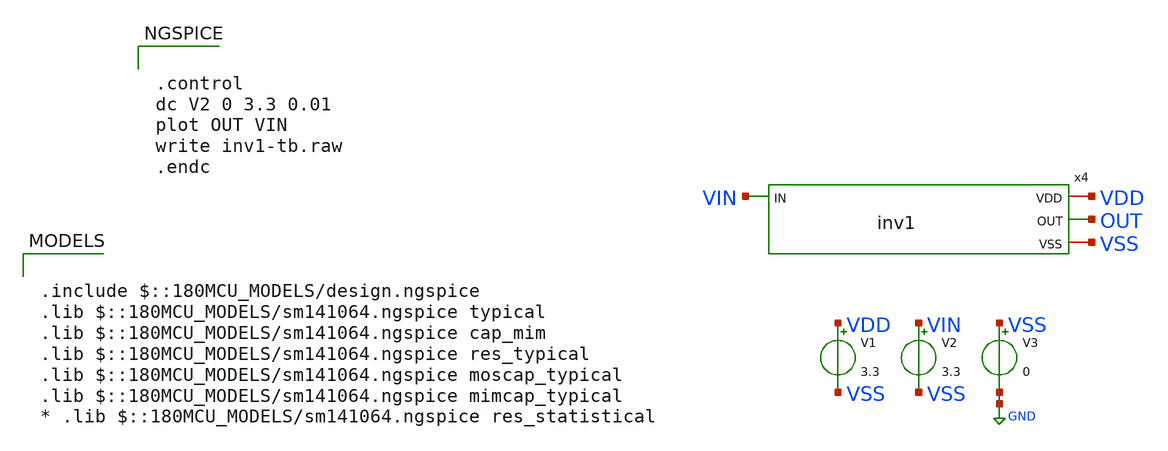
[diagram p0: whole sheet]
** sch_path: w1_advanced-foundation/w1_task/w1_inv-ring/inv1-tb.sch
**.subckt inv1-tb
V1 VDD VSS 3.3
V2 VIN VSS 3.3
V3 VSS GND 0
x4 VDD VIN OUT VSS inv1
**** begin user architecture code

.include $::180MCU_MODELS/design.ngspice
.lib $::180MCU_MODELS/sm141064.ngspice typical
.lib $::180MCU_MODELS/sm141064.ngspice cap_mim
.lib $::180MCU_MODELS/sm141064.ngspice res_typical
.lib $::180MCU_MODELS/sm141064.ngspice moscap_typical
.lib $::180MCU_MODELS/sm141064.ngspice mimcap_typical
* .lib $::180MCU_MODELS/sm141064.ngspice res_statistical



.control
dc V2 0 3.3 0.01
plot OUT VIN
write inv1-tb.raw
.endc


**** end user architecture code
**.ends

* expanding   symbol:  inv1.sym # of pins=4
** sym_path: w1_advanced-foundation/w1_task/w1_inv-ring/inv1.sym
** sch_path: w1_advanced-foundation/w1_task/w1_inv-ring/inv1.sch
.subckt inv1 VDD IN OUT VSS
*.iopin VDD
*.iopin VSS
*.ipin IN
*.opin OUT
XM2 OUT IN VDD VDD pfet_03v3 L=0.28u W=0.22u nf=1 ad='int((nf+1)/2) * W/nf * 0.18u' as='int((nf+2)/2) * W/nf * 0.18u'
+ pd='2*int((nf+1)/2) * (W/nf + 0.18u)' ps='2*int((nf+2)/2) * (W/nf + 0.18u)' nrd='0.18u / W' nrs='0.18u / W'
+ sa=0 sb=0 sd=0 m=3
XM1 OUT IN VSS VSS nfet_03v3 L=0.28u W=0.22u nf=1 ad='int((nf+1)/2) * W/nf * 0.18u' as='int((nf+2)/2) * W/nf * 0.18u'
+ pd='2*int((nf+1)/2) * (W/nf + 0.18u)' ps='2*int((nf+2)/2) * (W/nf + 0.18u)' nrd='0.18u / W' nrs='0.18u / W'
+ sa=0 sb=0 sd=0 m=1
.ends

.GLOBAL GND
.end
